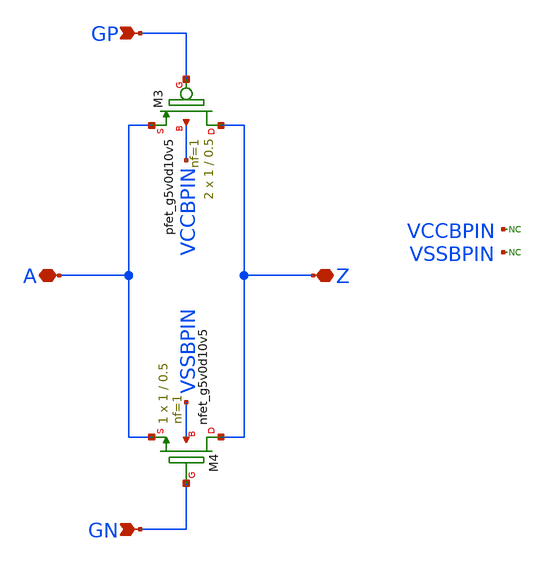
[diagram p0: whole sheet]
** sch_path: xschem/passgate_3p3.sch
* Copyright 2021 Stefan Frederik Schippers
* Licensed under the Apache License, Version 2.0 (the "License");
* you may not use this file except in compliance with the License.
* You may obtain a copy of the License at
* https://www.apache.org/licenses/LICENSE-2.0
* Unless required by applicable law or agreed to in writing, software
* distributed under the License is distributed on an "AS IS" BASIS,
* WITHOUT WARRANTIES OR CONDITIONS OF ANY KIND, either express or implied.
* See the License for the specific language governing permissions and
* limitations under the License.
**.subckt passgate_3p3 A Z GP GN
*.iopin A
*.iopin Z
*.ipin GP
*.ipin GN
* noconn VCCBPIN
* noconn VSSBPIN
XM3 Z GP A VCCBPIN sky130_fd_pr__pfet_g5v0d10v5 L=0.5 W=1 nf=1 ad='int((nf+1)/2) * W/nf * 0.29' as='int((nf+2)/2) * W/nf * 0.29'
+ pd='2*int((nf+1)/2) * (W/nf + 0.29)' ps='2*int((nf+2)/2) * (W/nf + 0.29)' nrd='0.29 / W' nrs='0.29 / W'
+ sa=0 sb=0 sd=0 mult=2 m=2
XM4 Z GN A VSSBPIN sky130_fd_pr__nfet_g5v0d10v5 L=0.5 W=1 nf=1 ad='int((nf+1)/2) * W/nf * 0.29' as='int((nf+2)/2) * W/nf * 0.29'
+ pd='2*int((nf+1)/2) * (W/nf + 0.29)' ps='2*int((nf+2)/2) * (W/nf + 0.29)' nrd='0.29 / W' nrs='0.29 / W'
+ sa=0 sb=0 sd=0 mult=1 m=1
**.ends
.end
